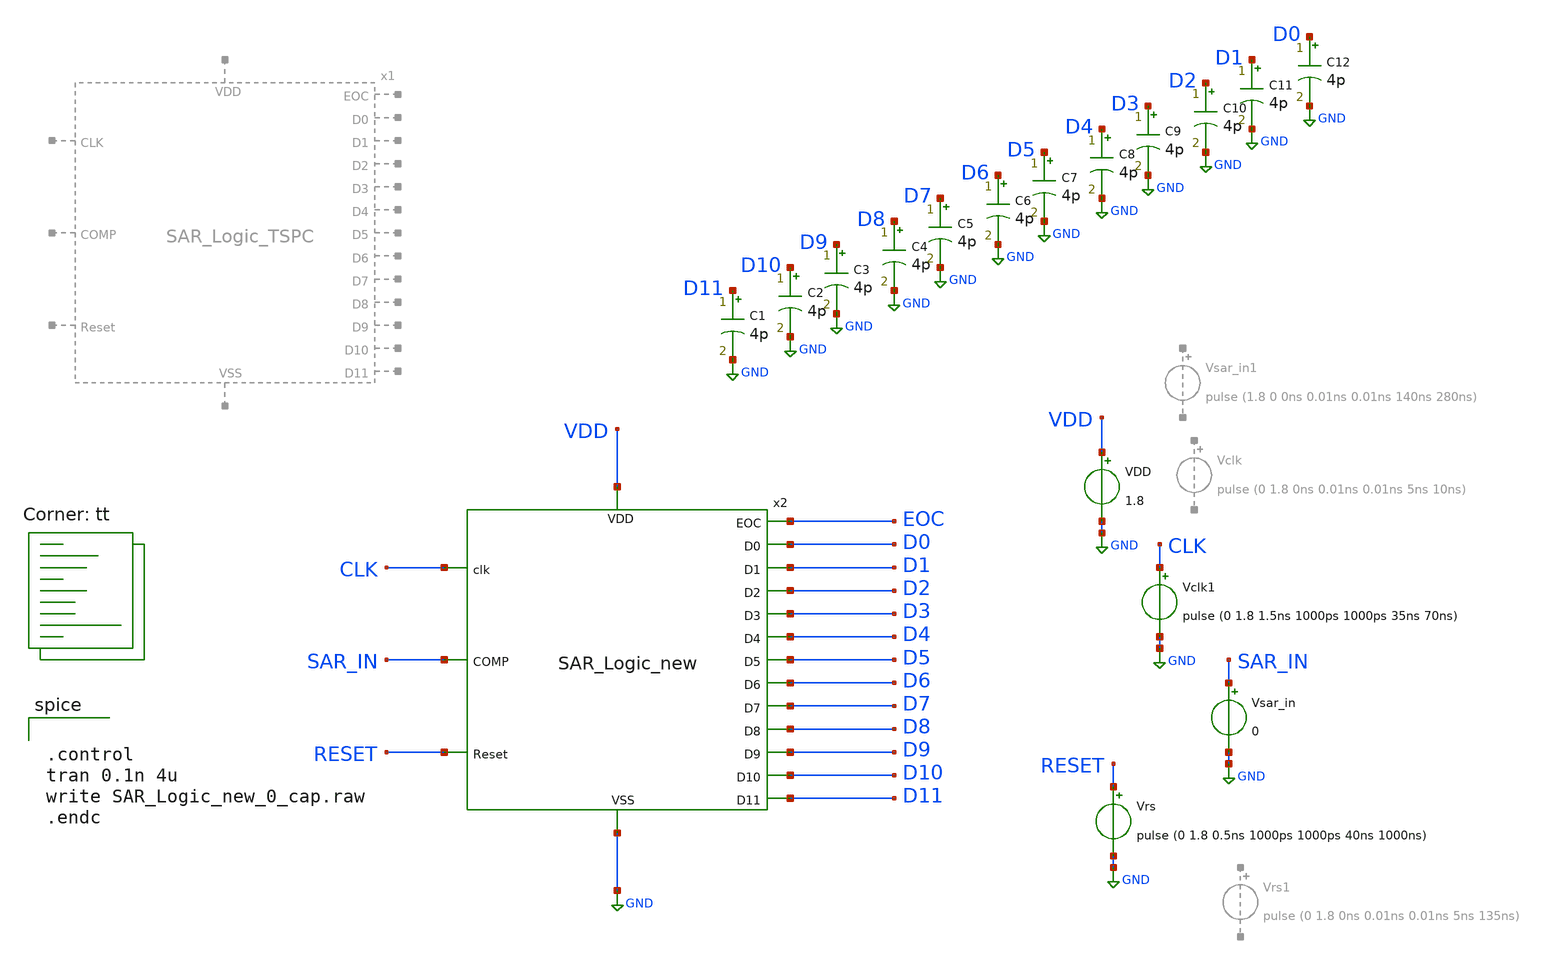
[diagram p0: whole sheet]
** sch_path: SAR_Logic_TSPC_tb.sch
**.subckt SAR_Logic_TSPC_tb
VDD VDD GND 1.8
Vsar_in SAR_IN GND 0
Vrs RESET GND pulse (0 1.8 0.5ns 1000ps 1000ps 40ns 1000ns)
Vclk1 CLK GND pulse (0 1.8 1.5ns 1000ps 1000ps 35ns 70ns)
x2 EOC CLK SAR_IN VDD GND RESET D9 D4 D10 D5 D6 D3 D2 D1 D0 D7 D8 D11 SAR_Logic_new
C1 D11 GND 4p m=1
C2 D10 GND 4p m=1
C3 D9 GND 4p m=1
C4 D8 GND 4p m=1
C5 D7 GND 4p m=1
C6 D6 GND 4p m=1
C7 D5 GND 4p m=1
C8 D4 GND 4p m=1
C9 D3 GND 4p m=1
C10 D2 GND 4p m=1
C11 D1 GND 4p m=1
C12 D0 GND 4p m=1
**** begin user architecture code
.lib $::SKYWATER_MODELS/sky130.lib.spice tt


.control
tran 0.1n 4u
write SAR_Logic_new_0_cap.raw
.endc

**** end user architecture code
**.ends

* expanding   symbol:  project/SAR_Logic_TSPC.sym # of pins=18
** sym_path: SAR_Logic_TSPC.sym
** sch_path: SAR_Logic_TSPC.sch
.subckt SAR_Logic_TSPC EOC CLK COMP VDD VSS Reset D9 D4 D10 D5 D6 D3 D2 D1 D0 D7 D8 D11
*.ipin CLK
*.ipin VDD
*.ipin VSS
*.ipin COMP
*.opin D11
*.opin D10
*.opin D9
*.opin D8
*.opin D7
*.opin D6
*.opin D5
*.opin D4
*.opin D3
*.opin D2
*.opin D1
*.opin D0
*.ipin Reset
*.opin EOC
x1 VDD VSS net2 D10 Reset COMP D11 FFD_TSPC
x2 VDD VSS net3 D9 Reset COMP D10 FFD_TSPC
x3 VDD VSS net4 D8 Reset COMP D9 FFD_TSPC
x4 VDD VSS net5 D7 Reset COMP D8 FFD_TSPC
x5 VDD VSS net6 D6 Reset COMP D7 FFD_TSPC
x6 VDD VSS net7 D5 Reset COMP D6 FFD_TSPC
x7 VDD VSS net8 D4 Reset COMP D5 FFD_TSPC
x8 VDD VSS net9 D3 Reset COMP D4 FFD_TSPC
x9 VDD VSS net10 D2 Reset COMP D3 FFD_TSPC
x10 VDD VSS net11 D1 Reset COMP D2 FFD_TSPC
x11 VDD VSS net12 D0 Reset COMP D1 FFD_TSPC
x12 VDD VSS net14 net13 Reset COMP D0 FFD_TSPC
x13 VDD VSS EOC VSS Reset VSS net13 FFD_TSPC
x14 VDD VSS Reset CLK VSS VSS net1 FFD_TSPC
x15 VDD VSS VSS CLK Reset net1 net2 FFD_TSPC
x16 VDD VSS VSS CLK Reset net2 net3 FFD_TSPC
x17 VDD VSS VSS CLK Reset net3 net4 FFD_TSPC
x18 VDD VSS VSS CLK Reset net4 net5 FFD_TSPC
x19 VDD VSS VSS CLK Reset net5 net6 FFD_TSPC
x20 VDD VSS VSS CLK Reset net6 net7 FFD_TSPC
x21 VDD VSS VSS CLK Reset net7 net8 FFD_TSPC
x22 VDD VSS VSS CLK Reset net8 net9 FFD_TSPC
x23 VDD VSS VSS CLK Reset net9 net10 FFD_TSPC
x24 VDD VSS VSS CLK Reset net10 net11 FFD_TSPC
x25 VDD VSS VSS CLK Reset net11 net12 FFD_TSPC
x26 VDD VSS VSS CLK Reset net12 net14 FFD_TSPC
x28 VDD VSS VSS CLK Reset net14 EOC FFD_TSPC
.ends


* expanding   symbol:  Thesis/SAR_Logic_new.sym # of pins=18
** sym_path: SAR_Logic_new.sym
** sch_path: SAR_Logic_new.sch
.subckt SAR_Logic_new EOC clk COMP VDD VSS Reset D9 D4 D10 D5 D6 D3 D2 D1 D0 D7 D8 D11
*.ipin VDD
*.ipin VSS
*.ipin COMP
*.ipin Reset
*.ipin clk
*.opin D11
*.opin D10
*.opin D9
*.opin D8
*.opin D7
*.opin D6
*.opin D5
*.opin D4
*.opin D3
*.opin D2
*.opin D1
*.opin D0
*.opin EOC
x1 Reset VDD net1 clk VSS VSS VSS FFD_logic_RS
x2 VSS VDD net2 clk net1 VSS Reset FFD_logic_RS
x3 VSS VDD net3 clk net2 VSS Reset FFD_logic_RS
x4 VSS VDD net4 clk net3 VSS Reset FFD_logic_RS
x5 VSS VDD net5 clk net4 VSS Reset FFD_logic_RS
x6 VSS VDD net6 clk net5 VSS Reset FFD_logic_RS
x7 VSS VDD net7 clk net6 VSS Reset FFD_logic_RS
x8 VSS VDD net8 clk net7 VSS Reset FFD_logic_RS
x9 VSS VDD net9 clk net8 VSS Reset FFD_logic_RS
x10 VSS VDD net10 clk net9 VSS Reset FFD_logic_RS
x11 VSS VDD net11 clk net10 VSS Reset FFD_logic_RS
x12 VSS VDD net12 clk net11 VSS Reset FFD_logic_RS
x13 VSS VDD net13 clk net12 VSS Reset FFD_logic_RS
x14 VSS VDD EOC clk net13 VSS Reset FFD_logic_RS
x15 net2 VDD D11 D10 COMP VSS Reset FFD_logic_RS
x16 net3 VDD D10 D9 COMP VSS Reset FFD_logic_RS
x17 net4 VDD D9 D8 COMP VSS Reset FFD_logic_RS
x18 net5 VDD D8 D7 COMP VSS Reset FFD_logic_RS
x19 net6 VDD D7 D6 COMP VSS Reset FFD_logic_RS
x20 net7 VDD D6 D5 COMP VSS Reset FFD_logic_RS
x21 net8 VDD D5 D4 COMP VSS Reset FFD_logic_RS
x22 net9 VDD D4 D3 COMP VSS Reset FFD_logic_RS
x23 net10 VDD D3 D2 COMP VSS Reset FFD_logic_RS
x24 net11 VDD D2 D1 COMP VSS Reset FFD_logic_RS
x25 net12 VDD D1 D0 COMP VSS Reset FFD_logic_RS
x26 net13 VDD D0 net14 COMP VSS Reset FFD_logic_RS
x27 EOC VDD net14 VSS VSS VSS Reset FFD_logic_RS
.ends


* expanding   symbol:  FFD_TSPC.sym # of pins=7
** sym_path: FFD_TSPC.sym
** sch_path: FFD_TSPC.sch
.subckt FFD_TSPC VDD VSS SET CLOCK RESET D Q
*.ipin CLOCK
*.ipin SET
*.ipin RESET
*.ipin VDD
*.ipin VSS
*.ipin D
*.opin Q
XM1 net2 D VSS VSS sky130_fd_pr__nfet_01v8 L=0.15 W=0.5 nf=1 ad='int((nf+1)/2) * W/nf * 0.29' as='int((nf+2)/2) * W/nf * 0.29'
+ pd='2*int((nf+1)/2) * (W/nf + 0.29)' ps='2*int((nf+2)/2) * (W/nf + 0.29)' nrd='0.29 / W' nrs='0.29 / W'
+ sa=0 sb=0 sd=0 mult=1 m=1
XM2 net3 CLOCK VSS VSS sky130_fd_pr__nfet_01v8 L=0.15 W=0.5 nf=1 ad='int((nf+1)/2) * W/nf * 0.29' as='int((nf+2)/2) * W/nf * 0.29'
+ pd='2*int((nf+1)/2) * (W/nf + 0.29)' ps='2*int((nf+2)/2) * (W/nf + 0.29)' nrd='0.29 / W' nrs='0.29 / W'
+ sa=0 sb=0 sd=0 mult=1 m=1
XM3 net4 Q_pre VSS VSS sky130_fd_pr__nfet_01v8 L=0.15 W=0.5 nf=1 ad='int((nf+1)/2) * W/nf * 0.29' as='int((nf+2)/2) * W/nf * 0.29'
+ pd='2*int((nf+1)/2) * (W/nf + 0.29)' ps='2*int((nf+2)/2) * (W/nf + 0.29)' nrd='0.29 / W' nrs='0.29 / W'
+ sa=0 sb=0 sd=0 mult=1 m=1
XM4 net2 CLOCK net1 VDD sky130_fd_pr__pfet_01v8 L=0.15 W=2 nf=1 ad='int((nf+1)/2) * W/nf * 0.29' as='int((nf+2)/2) * W/nf * 0.29'
+ pd='2*int((nf+1)/2) * (W/nf + 0.29)' ps='2*int((nf+2)/2) * (W/nf + 0.29)' nrd='0.29 / W' nrs='0.29 / W'
+ sa=0 sb=0 sd=0 mult=1 m=1
XM5 Q_pre net2 net3 VSS sky130_fd_pr__nfet_01v8 L=0.15 W=0.5 nf=1 ad='int((nf+1)/2) * W/nf * 0.29' as='int((nf+2)/2) * W/nf * 0.29'
+ pd='2*int((nf+1)/2) * (W/nf + 0.29)' ps='2*int((nf+2)/2) * (W/nf + 0.29)' nrd='0.29 / W' nrs='0.29 / W'
+ sa=0 sb=0 sd=0 mult=1 m=1
XM6 QB_pre CLOCK net4 VSS sky130_fd_pr__nfet_01v8 L=0.15 W=0.5 nf=1 ad='int((nf+1)/2) * W/nf * 0.29'
+ as='int((nf+2)/2) * W/nf * 0.29' pd='2*int((nf+1)/2) * (W/nf + 0.29)' ps='2*int((nf+2)/2) * (W/nf + 0.29)'
+ nrd='0.29 / W' nrs='0.29 / W' sa=0 sb=0 sd=0 mult=1 m=1
XM7 Q QB_pre VSS VSS sky130_fd_pr__nfet_01v8 L=0.15 W=3 nf=1 ad='int((nf+1)/2) * W/nf * 0.29' as='int((nf+2)/2) * W/nf * 0.29'
+ pd='2*int((nf+1)/2) * (W/nf + 0.29)' ps='2*int((nf+2)/2) * (W/nf + 0.29)' nrd='0.29 / W' nrs='0.29 / W'
+ sa=0 sb=0 sd=0 mult=1 m=1
XM8 net1 D VDD VDD sky130_fd_pr__pfet_01v8 L=0.15 W=2 nf=1 ad='int((nf+1)/2) * W/nf * 0.29' as='int((nf+2)/2) * W/nf * 0.29'
+ pd='2*int((nf+1)/2) * (W/nf + 0.29)' ps='2*int((nf+2)/2) * (W/nf + 0.29)' nrd='0.29 / W' nrs='0.29 / W'
+ sa=0 sb=0 sd=0 mult=1 m=1
XM9 Q_pre CLOCK VDD VDD sky130_fd_pr__pfet_01v8 L=0.15 W=2 nf=1 ad='int((nf+1)/2) * W/nf * 0.29' as='int((nf+2)/2) * W/nf * 0.29'
+ pd='2*int((nf+1)/2) * (W/nf + 0.29)' ps='2*int((nf+2)/2) * (W/nf + 0.29)' nrd='0.29 / W' nrs='0.29 / W'
+ sa=0 sb=0 sd=0 mult=1 m=1
XM10 net5 Q_pre VDD VDD sky130_fd_pr__pfet_01v8 L=0.15 W=2 nf=1 ad='int((nf+1)/2) * W/nf * 0.29' as='int((nf+2)/2) * W/nf * 0.29'
+ pd='2*int((nf+1)/2) * (W/nf + 0.29)' ps='2*int((nf+2)/2) * (W/nf + 0.29)' nrd='0.29 / W' nrs='0.29 / W'
+ sa=0 sb=0 sd=0 mult=1 m=1
XM11 QB_pre RS VDD VDD sky130_fd_pr__pfet_01v8 L=0.15 W=2 nf=1 ad='int((nf+1)/2) * W/nf * 0.29' as='int((nf+2)/2) * W/nf * 0.29'
+ pd='2*int((nf+1)/2) * (W/nf + 0.29)' ps='2*int((nf+2)/2) * (W/nf + 0.29)' nrd='0.29 / W' nrs='0.29 / W'
+ sa=0 sb=0 sd=0 mult=1 m=1
XM12 Q QB_pre VDD VDD sky130_fd_pr__pfet_01v8 L=0.15 W=6 nf=1 ad='int((nf+1)/2) * W/nf * 0.29' as='int((nf+2)/2) * W/nf * 0.29'
+ pd='2*int((nf+1)/2) * (W/nf + 0.29)' ps='2*int((nf+2)/2) * (W/nf + 0.29)' nrd='0.29 / W' nrs='0.29 / W'
+ sa=0 sb=0 sd=0 mult=1 m=1
XM13 QB_pre SET VSS VSS sky130_fd_pr__nfet_01v8 L=0.15 W=0.5 nf=1 ad='int((nf+1)/2) * W/nf * 0.29' as='int((nf+2)/2) * W/nf * 0.29'
+ pd='2*int((nf+1)/2) * (W/nf + 0.29)' ps='2*int((nf+2)/2) * (W/nf + 0.29)' nrd='0.29 / W' nrs='0.29 / W'
+ sa=0 sb=0 sd=0 mult=1 m=1
x1 VDD RESET RS VSS Inverter
XM14 QB_pre SET net5 VDD sky130_fd_pr__pfet_01v8 L=0.15 W=2 nf=1 ad='int((nf+1)/2) * W/nf * 0.29' as='int((nf+2)/2) * W/nf * 0.29'
+ pd='2*int((nf+1)/2) * (W/nf + 0.29)' ps='2*int((nf+2)/2) * (W/nf + 0.29)' nrd='0.29 / W' nrs='0.29 / W'
+ sa=0 sb=0 sd=0 mult=1 m=1
.ends


* expanding   symbol:  Thesis/FFD_logic_RS.sym # of pins=7
** sym_path: FFD_logic_RS.sym
** sch_path: FFD_logic_RS.sch
.subckt FFD_logic_RS Set VDD Q CLK D VSS Reset
*.ipin D
*.ipin CLK
*.ipin VDD
*.ipin VSS
*.opin Q
*.ipin Set
*.ipin Reset
x1 VDD net3 D net2 VSS nand_FFD
x2 VDD net4 net2 net1 VSS nand_FFD
x5 VDD net8 net5 CLK VSS nand_FFD
x6 VDD net7 CLK net6 VSS nand_FFD
x9 VDD D net1 VSS Inverter
x10 VDD CLK net2 VSS Inverter
x3 net6 VDD net5 net10 net3 VSS nand_FFD_3pin
x4 net11 VDD net6 net5 net4 VSS nand_FFD_3pin
x7 net9 VDD Q net10 net8 VSS nand_FFD_3pin
x8 net11 VDD net9 Q net7 VSS nand_FFD_3pin
x11 VDD Set net10 VSS Inverter
x12 VDD Reset net11 VSS Inverter
.ends


* expanding   symbol:  Inverter.sym # of pins=4
** sym_path: Inverter.sym
** sch_path: Inverter.sch
.subckt Inverter VDD IN OUT VSS
*.ipin IN
*.ipin VSS
*.ipin VDD
*.opin OUT
XM1 OUT IN VSS VSS sky130_fd_pr__nfet_01v8 L=0.3 W=1 nf=1 ad='int((nf+1)/2) * W/nf * 0.29' as='int((nf+2)/2) * W/nf * 0.29'
+ pd='2*int((nf+1)/2) * (W/nf + 0.29)' ps='2*int((nf+2)/2) * (W/nf + 0.29)' nrd='0.29 / W' nrs='0.29 / W'
+ sa=0 sb=0 sd=0 mult=1 m=1
XM2 OUT IN VDD VDD sky130_fd_pr__pfet_01v8 L=0.3 W=2 nf=1 ad='int((nf+1)/2) * W/nf * 0.29' as='int((nf+2)/2) * W/nf * 0.29'
+ pd='2*int((nf+1)/2) * (W/nf + 0.29)' ps='2*int((nf+2)/2) * (W/nf + 0.29)' nrd='0.29 / W' nrs='0.29 / W'
+ sa=0 sb=0 sd=0 mult=1 m=1
.ends


* expanding   symbol:  nand_FFD.sym # of pins=5
** sym_path: nand_FFD.sym
** sch_path: nand_FFD.sch
.subckt nand_FFD VDD Y A B VSS
*.ipin VDD
*.ipin A
*.ipin B
*.ipin VSS
*.opin Y
XM1 Y A net1 VSS sky130_fd_pr__nfet_01v8 L=0.15 W=1 nf=1 ad='int((nf+1)/2) * W/nf * 0.29' as='int((nf+2)/2) * W/nf * 0.29'
+ pd='2*int((nf+1)/2) * (W/nf + 0.29)' ps='2*int((nf+2)/2) * (W/nf + 0.29)' nrd='0.29 / W' nrs='0.29 / W'
+ sa=0 sb=0 sd=0 mult=1 m=1
XM2 net1 B VSS VSS sky130_fd_pr__nfet_01v8 L=0.15 W=1 nf=1 ad='int((nf+1)/2) * W/nf * 0.29' as='int((nf+2)/2) * W/nf * 0.29'
+ pd='2*int((nf+1)/2) * (W/nf + 0.29)' ps='2*int((nf+2)/2) * (W/nf + 0.29)' nrd='0.29 / W' nrs='0.29 / W'
+ sa=0 sb=0 sd=0 mult=1 m=1
XM3 Y A VDD VDD sky130_fd_pr__pfet_01v8 L=0.15 W=2 nf=1 ad='int((nf+1)/2) * W/nf * 0.29' as='int((nf+2)/2) * W/nf * 0.29'
+ pd='2*int((nf+1)/2) * (W/nf + 0.29)' ps='2*int((nf+2)/2) * (W/nf + 0.29)' nrd='0.29 / W' nrs='0.29 / W'
+ sa=0 sb=0 sd=0 mult=1 m=1
XM4 Y B VDD VDD sky130_fd_pr__pfet_01v8 L=0.15 W=2 nf=1 ad='int((nf+1)/2) * W/nf * 0.29' as='int((nf+2)/2) * W/nf * 0.29'
+ pd='2*int((nf+1)/2) * (W/nf + 0.29)' ps='2*int((nf+2)/2) * (W/nf + 0.29)' nrd='0.29 / W' nrs='0.29 / W'
+ sa=0 sb=0 sd=0 mult=1 m=1
.ends


* expanding   symbol:  Thesis/nand_FFD_3pin.sym # of pins=6
** sym_path: nand_FFD_3pin.sym
** sch_path: nand_FFD_3pin.sch
.subckt nand_FFD_3pin C VDD Y A B VSS
*.ipin VDD
*.ipin A
*.ipin B
*.ipin VSS
*.opin Y
*.ipin C
XM1 Y A net1 VSS sky130_fd_pr__nfet_01v8 L=0.15 W=1 nf=1 ad='int((nf+1)/2) * W/nf * 0.29' as='int((nf+2)/2) * W/nf * 0.29'
+ pd='2*int((nf+1)/2) * (W/nf + 0.29)' ps='2*int((nf+2)/2) * (W/nf + 0.29)' nrd='0.29 / W' nrs='0.29 / W'
+ sa=0 sb=0 sd=0 mult=1 m=1
XM2 net1 B net2 VSS sky130_fd_pr__nfet_01v8 L=0.15 W=1 nf=1 ad='int((nf+1)/2) * W/nf * 0.29' as='int((nf+2)/2) * W/nf * 0.29'
+ pd='2*int((nf+1)/2) * (W/nf + 0.29)' ps='2*int((nf+2)/2) * (W/nf + 0.29)' nrd='0.29 / W' nrs='0.29 / W'
+ sa=0 sb=0 sd=0 mult=1 m=1
XM3 Y A VDD VDD sky130_fd_pr__pfet_01v8 L=0.15 W=2 nf=1 ad='int((nf+1)/2) * W/nf * 0.29' as='int((nf+2)/2) * W/nf * 0.29'
+ pd='2*int((nf+1)/2) * (W/nf + 0.29)' ps='2*int((nf+2)/2) * (W/nf + 0.29)' nrd='0.29 / W' nrs='0.29 / W'
+ sa=0 sb=0 sd=0 mult=1 m=1
XM4 Y B VDD VDD sky130_fd_pr__pfet_01v8 L=0.15 W=2 nf=1 ad='int((nf+1)/2) * W/nf * 0.29' as='int((nf+2)/2) * W/nf * 0.29'
+ pd='2*int((nf+1)/2) * (W/nf + 0.29)' ps='2*int((nf+2)/2) * (W/nf + 0.29)' nrd='0.29 / W' nrs='0.29 / W'
+ sa=0 sb=0 sd=0 mult=1 m=1
XM5 Y C VDD VDD sky130_fd_pr__pfet_01v8 L=0.15 W=2 nf=1 ad='int((nf+1)/2) * W/nf * 0.29' as='int((nf+2)/2) * W/nf * 0.29'
+ pd='2*int((nf+1)/2) * (W/nf + 0.29)' ps='2*int((nf+2)/2) * (W/nf + 0.29)' nrd='0.29 / W' nrs='0.29 / W'
+ sa=0 sb=0 sd=0 mult=1 m=1
XM6 net2 C VSS VSS sky130_fd_pr__nfet_01v8 L=0.15 W=1 nf=1 ad='int((nf+1)/2) * W/nf * 0.29' as='int((nf+2)/2) * W/nf * 0.29'
+ pd='2*int((nf+1)/2) * (W/nf + 0.29)' ps='2*int((nf+2)/2) * (W/nf + 0.29)' nrd='0.29 / W' nrs='0.29 / W'
+ sa=0 sb=0 sd=0 mult=1 m=1
.ends

.GLOBAL GND
.end
